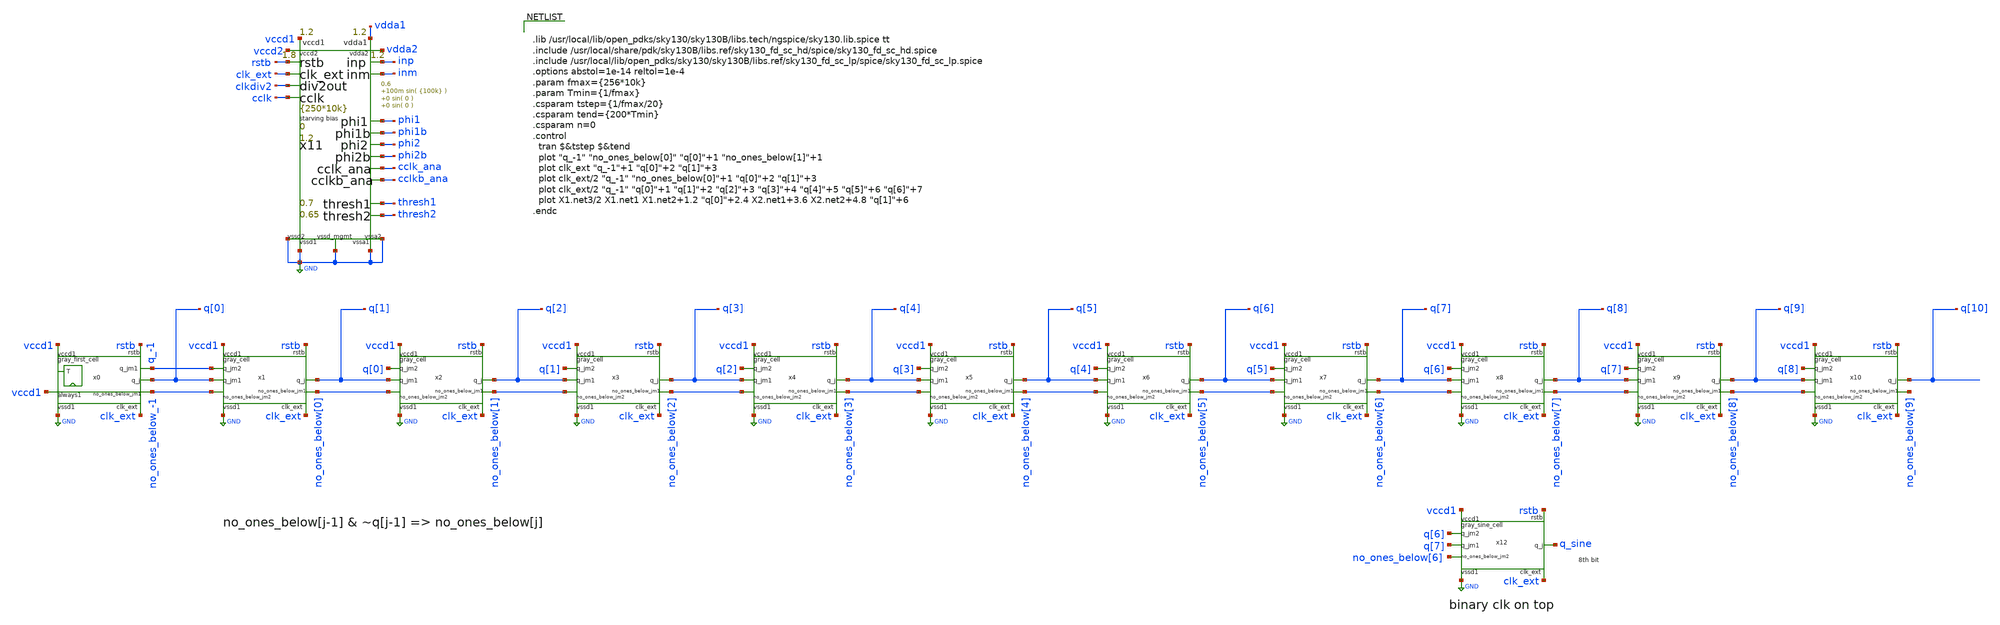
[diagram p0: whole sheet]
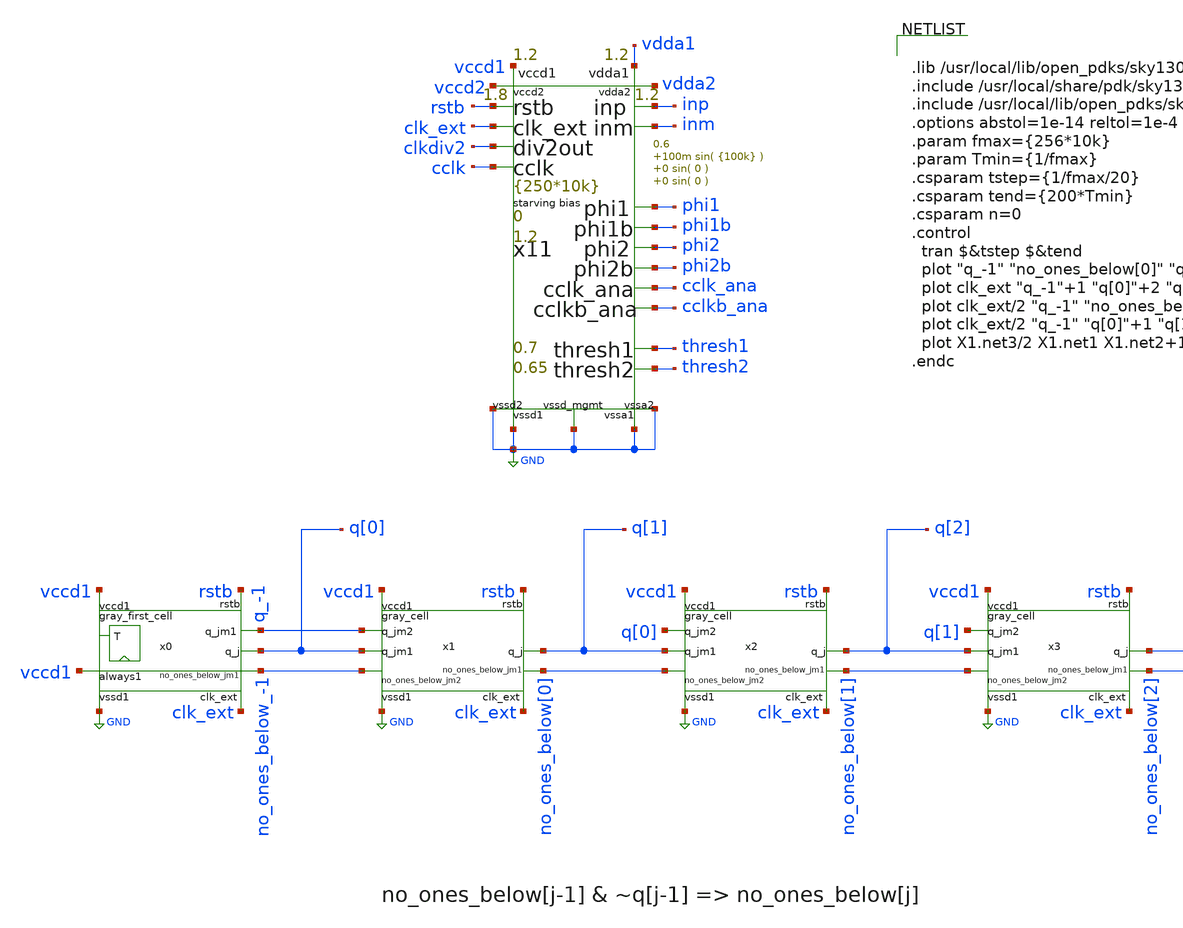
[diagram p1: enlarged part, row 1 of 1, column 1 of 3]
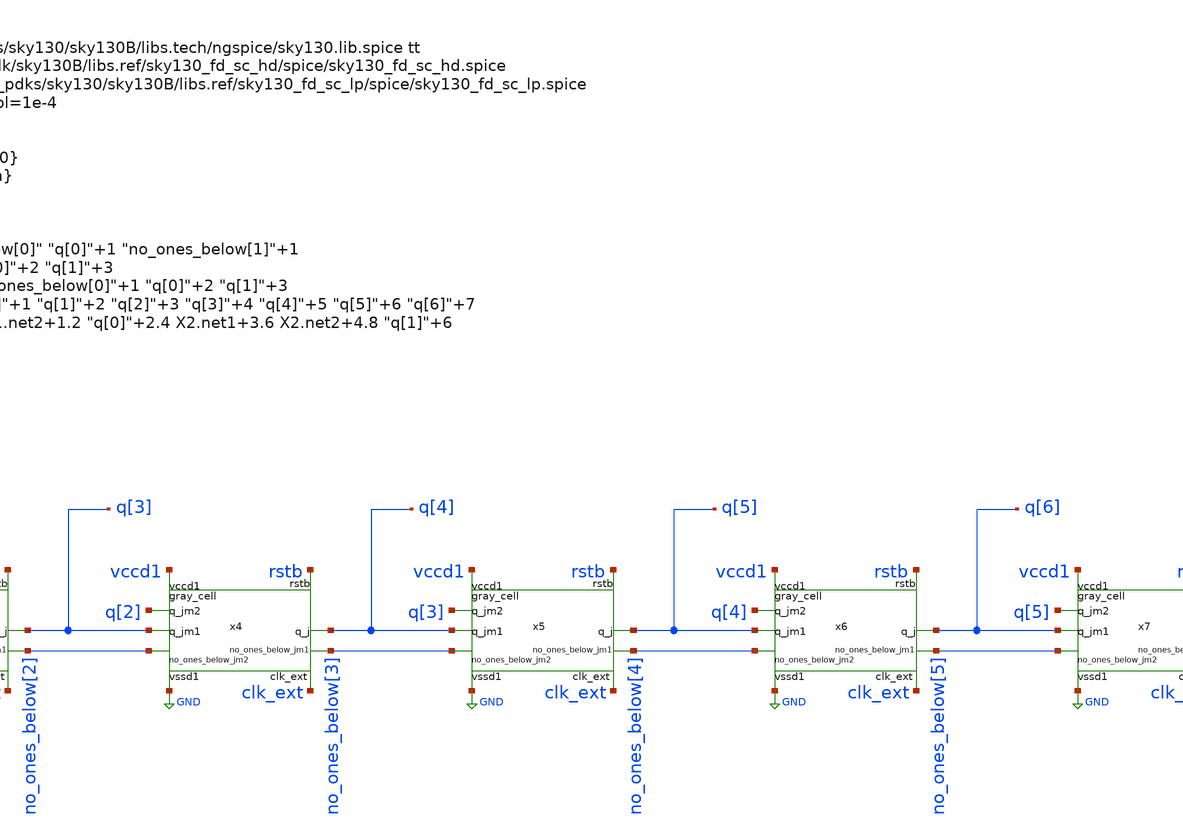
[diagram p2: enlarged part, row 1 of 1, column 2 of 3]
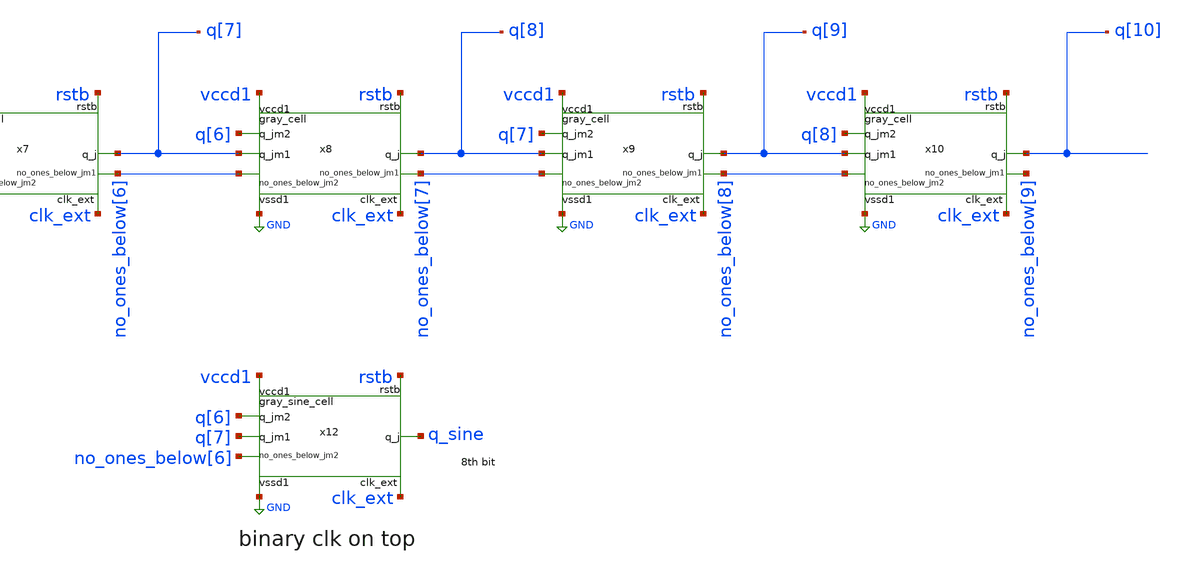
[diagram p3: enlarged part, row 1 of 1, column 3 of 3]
** sch_path: xschem/test_bench/gray_counter_dff_tb.sch
**.subckt gray_counter_dff_tb
x11 thresh1 thresh2 inp inm clk_ext rstb phi1 phi1 phi1b phi1b phi2 phi2 phi2b phi2b cclk_ana cclk_ana
+ cclkb_ana cclkb_ana clkdiv2 clkdiv2 cclk cclk vdda1 vccd1 vccd2 vdda2 GND GND GND GND GND risc_signals
+ p_vdda1=1.2 p_vdda2=1.2 p_vccd1=1.2 p_vccd2=1.8 p_vccd_mgmt=1.8 p_fclk={250*10k} p_duty_cycle=0.5 p_rstb_delay={1.5/p_fclk}
+ p_rstb_tr=5n p_thresh1=0.7 p_thresh2=0.65 p_vpb=0 p_vnb=1.2 p_vcm=0.6 p_amp1=100m p_f1={100k} p_amp2=0
+ p_f2=0 p_amp3=0 p_f3=0
x0 clk_ext q_-1 rstb vccd1 GND vccd1 no_ones_below_-1 q[0] gray_first_cell
x1 clk_ext q[1] rstb vccd1 GND no_ones_below[0] no_ones_below_-1 q[0] q_-1 gray_cell
x2 clk_ext q[2] rstb vccd1 GND no_ones_below[1] no_ones_below[0] q[1] q[0] gray_cell
x3 clk_ext q[3] rstb vccd1 GND no_ones_below[2] no_ones_below[1] q[2] q[1] gray_cell
x4 clk_ext q[4] rstb vccd1 GND no_ones_below[3] no_ones_below[2] q[3] q[2] gray_cell
x5 clk_ext q[5] rstb vccd1 GND no_ones_below[4] no_ones_below[3] q[4] q[3] gray_cell
x6 clk_ext q[6] rstb vccd1 GND no_ones_below[5] no_ones_below[4] q[5] q[4] gray_cell
x7 clk_ext q[7] rstb vccd1 GND no_ones_below[6] no_ones_below[5] q[6] q[5] gray_cell
x8 clk_ext q[8] rstb vccd1 GND no_ones_below[7] no_ones_below[6] q[7] q[6] gray_cell
x9 clk_ext q[9] rstb vccd1 GND no_ones_below[8] no_ones_below[7] q[8] q[7] gray_cell
x10 clk_ext q[10] rstb vccd1 GND no_ones_below[9] no_ones_below[8] q[9] q[8] gray_cell
x12 clk_ext q_sine rstb vccd1 GND no_ones_below[6] q[7] q[6] gray_sine_cell
**** begin user architecture code


.lib /usr/local/lib/open_pdks/sky130/sky130B/libs.tech/ngspice/sky130.lib.spice tt
.include /usr/local/share/pdk/sky130B/libs.ref/sky130_fd_sc_hd/spice/sky130_fd_sc_hd.spice
.include /usr/local/lib/open_pdks/sky130/sky130B/libs.ref/sky130_fd_sc_lp/spice/sky130_fd_sc_lp.spice
.options abstol=1e-14 reltol=1e-4
.param fmax={256*10k}
.param Tmin={1/fmax}
.csparam tstep={1/fmax/20}
.csparam tend={200*Tmin}
.csparam n=0
.control
  tran $&tstep $&tend
  plot "q_-1" "no_ones_below[0]" "q[0]"+1 "no_ones_below[1]"+1
  plot clk_ext "q_-1"+1 "q[0]"+2 "q[1]"+3
  plot clk_ext/2 "q_-1" "no_ones_below[0]"+1 "q[0]"+2 "q[1]"+3
  plot clk_ext/2 "q_-1" "q[0]"+1 "q[1]"+2 "q[2]"+3 "q[3]"+4 "q[4]"+5 "q[5]"+6 "q[6]"+7
  plot X1.net3/2 X1.net1 X1.net2+1.2 "q[0]"+2.4 X2.net1+3.6 X2.net2+4.8 "q[1]"+6
.endc


**** end user architecture code
**.ends
.GLOBAL GND
.end
